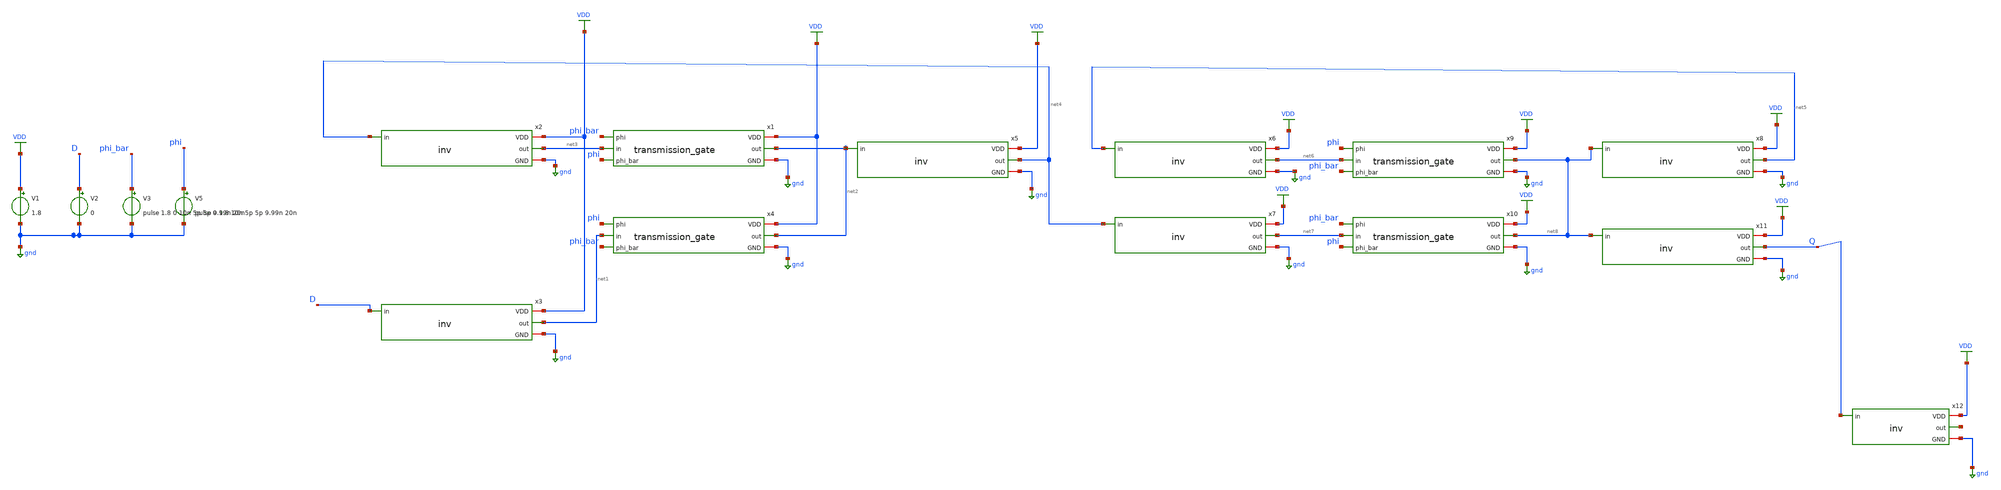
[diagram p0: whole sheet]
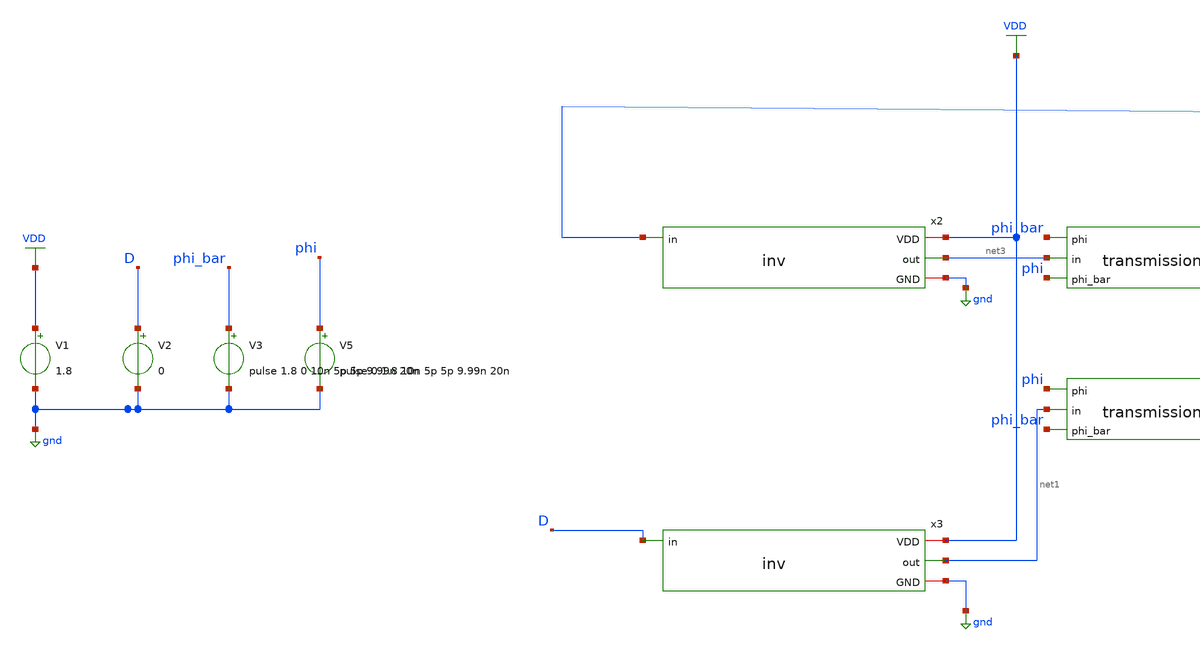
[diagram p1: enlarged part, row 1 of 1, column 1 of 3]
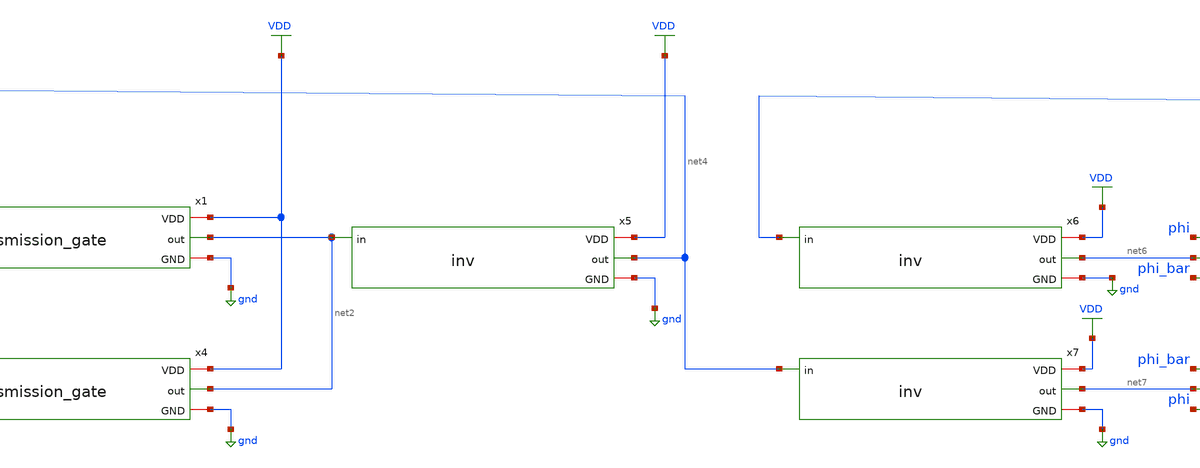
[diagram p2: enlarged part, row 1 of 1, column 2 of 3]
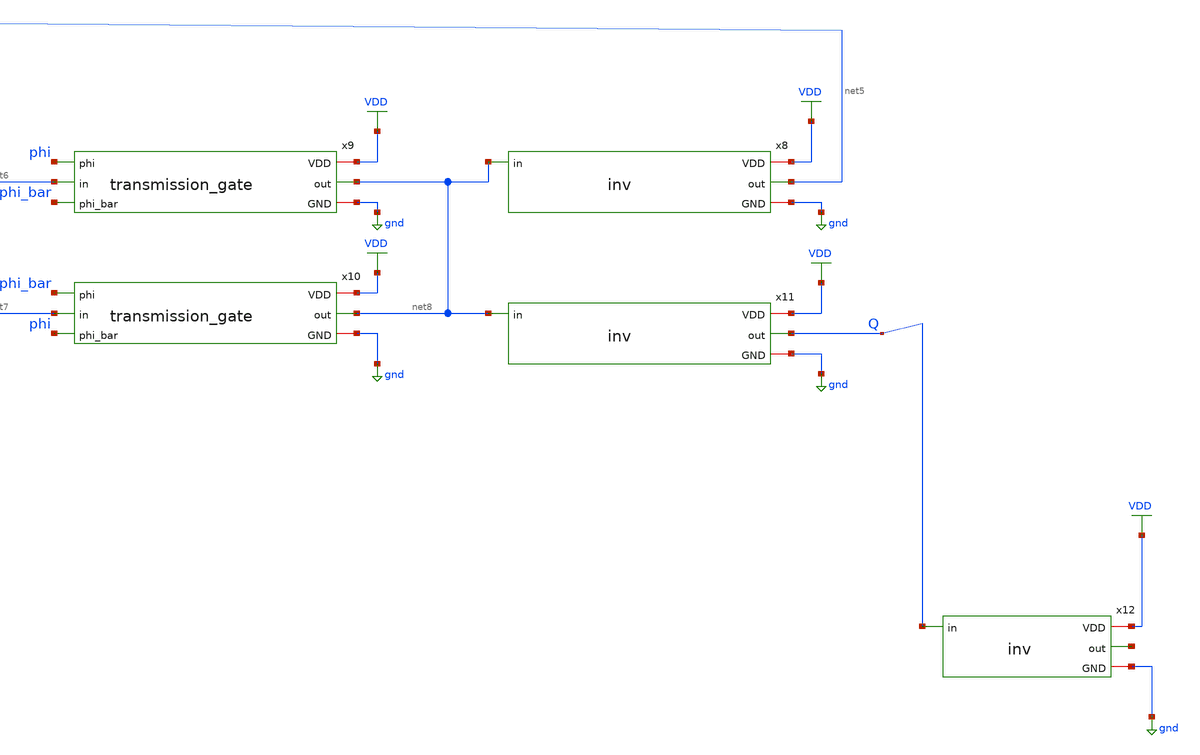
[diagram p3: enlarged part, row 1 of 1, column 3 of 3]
** sch_path: assignments/assignment6/assign1b.sch
**.subckt assign1b
V1 VDD gnd 1.8
V2 D gnd 0
V3 phi_bar gnd pulse 1.8 0 10n 5p 5p 9.99n 20n
V5 phi gnd pulse 0 1.8 10n 5p 5p 9.99n 20n
x1 phi_bar VDD net3 net2 gnd phi transmission_gate
x2 VDD net4 net3 gnd inv
x3 VDD D net1 gnd inv
x4 phi VDD net1 net2 gnd phi_bar transmission_gate
x5 VDD net2 net4 gnd inv
x6 VDD net5 net6 gnd inv
x7 VDD net4 net7 gnd inv
x8 VDD net8 net5 gnd inv
x9 phi VDD net6 net8 gnd phi_bar transmission_gate
x10 phi_bar VDD net7 net8 gnd phi transmission_gate
x11 VDD net8 Q gnd inv
x12 VDD Q net9 gnd inv
**** begin user architecture code
.lib $::SKYWATER_MODELS/sky130.lib.spice tt


.control
* Initialize variables for the sweep
let t_start = 9.5n
let t_step = 10p
let t_stop = 9.88n
let current_t = t_start

let min_tdq = 1
let opt_setup = 0
let opt_tcq = 0

let n_pts = floor((t_stop - t_start) / t_step)
let tdc_sweep = unitvec(n_pts)
let tcq_sweep = tdc_sweep * 0
let tdq_sweep = tdc_sweep * 0
let idx = 0

while current_t <= t_stop
    * Alter D input pulse delay
    alter @V2[pulse] = [ 1.8 0 $&current_t 5p 5p 10n 20n ]

    * Run transient analysis WITHOUT 'uic' so SPICE calculates the DC operating point
    tran 5p 15n

    * Measurements
    meas tran tdc TRIG v(D) VAL=0.9 FALL=1 TARG v(phi) VAL=0.9 RISE=1
    meas tran tcq TRIG v(phi) VAL=0.9 RISE=1 TARG v(Q) VAL=0.9 FALL=1 TD=10n
    meas tran tdq TRIG v(D) VAL=0.9 FALL=1 TARG v(Q) VAL=0.9 FALL=1 TD=10n

    let tdc_sweep[idx] = tdc
    if tcq > 0
        let tcq_sweep[idx] = tcq
    end
    if tdq > 0
        let tdq_sweep[idx] = tdq
    end

    * Safely check if tdq was measured successfully before comparing
    if length(tdq) > 0
        if tdq < min_tdq
            let min_tdq = tdq
            let opt_setup = tdc
            let opt_tcq = tcq
        end
    end

    let idx = idx + 1
    let current_t = current_t + t_step
end

print opt_setup opt_tcq min_tdq

* Setup-time sweep: tDQ and tCQ vs tsetup (native ngspice plot)
plot tdq_sweep tcq_sweep vs tdc_sweep
.endc


**** end user architecture code
**.ends

* expanding   symbol:  transmission_gate.sym # of pins=6
** sym_path: assignments/assignment6/transmission_gate.sym
** sch_path: assignments/assignment6/transmission_gate.sch
.subckt transmission_gate phi VDD in out GND phi_bar
*.ipin in
*.opin out
*.ipin phi
*.ipin phi_bar
*.iopin GND
*.iopin VDD
XM3 in phi_bar out GND sky130_fd_pr__nfet_01v8 L=0.15 W=0.42 nf=1 ad='int((nf+1)/2) * W/nf * 0.29' as='int((nf+2)/2) * W/nf * 0.29'
+ pd='2*int((nf+1)/2) * (W/nf + 0.29)' ps='2*int((nf+2)/2) * (W/nf + 0.29)' nrd='0.29 / W' nrs='0.29 / W'
+ sa=0 sb=0 sd=0 mult=1 m=1
XM4 in phi out VDD sky130_fd_pr__pfet_01v8 L=0.15 W=0.42 nf=1 ad='int((nf+1)/2) * W/nf * 0.29' as='int((nf+2)/2) * W/nf * 0.29'
+ pd='2*int((nf+1)/2) * (W/nf + 0.29)' ps='2*int((nf+2)/2) * (W/nf + 0.29)' nrd='0.29 / W' nrs='0.29 / W'
+ sa=0 sb=0 sd=0 mult=1 m=1
.ends


* expanding   symbol:  inv.sym # of pins=4
** sym_path: assignments/assignment6/inv.sym
** sch_path: assignments/assignment6/inv.sch
.subckt inv VDD in out GND
*.ipin in
*.iopin GND
*.iopin VDD
*.opin out
XM3 out in GND GND sky130_fd_pr__nfet_01v8 L=0.15 W=0.42 nf=1 ad='int((nf+1)/2) * W/nf * 0.29' as='int((nf+2)/2) * W/nf * 0.29'
+ pd='2*int((nf+1)/2) * (W/nf + 0.29)' ps='2*int((nf+2)/2) * (W/nf + 0.29)' nrd='0.29 / W' nrs='0.29 / W'
+ sa=0 sb=0 sd=0 mult=1 m=1
XM4 out in VDD VDD sky130_fd_pr__pfet_01v8 L=0.15 W=0.84 nf=1 ad='int((nf+1)/2) * W/nf * 0.29' as='int((nf+2)/2) * W/nf * 0.29'
+ pd='2*int((nf+1)/2) * (W/nf + 0.29)' ps='2*int((nf+2)/2) * (W/nf + 0.29)' nrd='0.29 / W' nrs='0.29 / W'
+ sa=0 sb=0 sd=0 mult=1 m=1
.ends

.GLOBAL VDD
.GLOBAL gnd
.end
